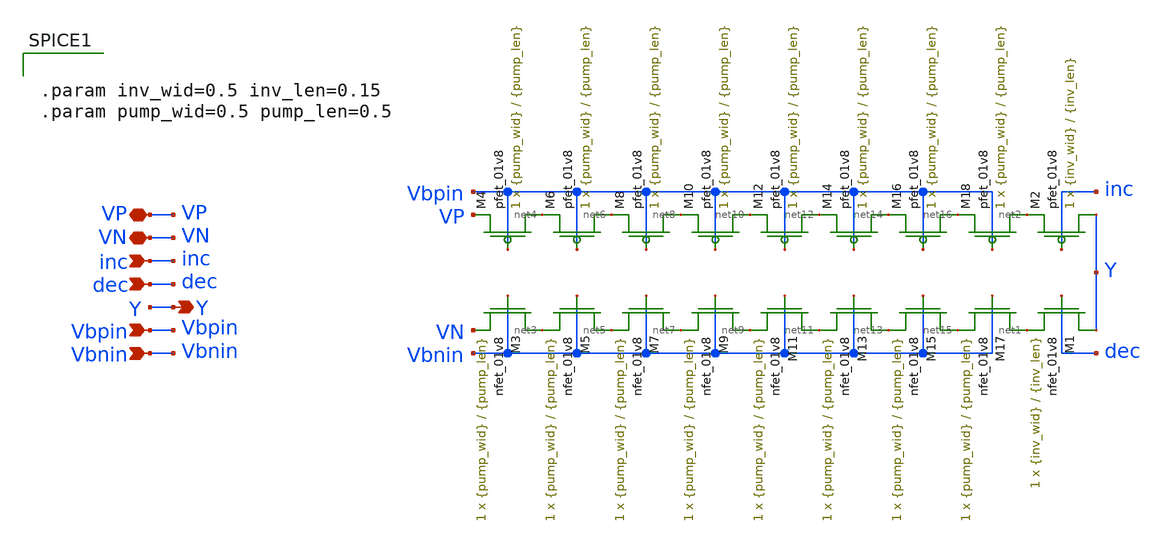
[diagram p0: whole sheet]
** sch_path: LDS/LDS_ipump.sch
**.subckt LDS_ipump VN VP Y Vbpin inc Vbnin dec
*.iopin VN
*.iopin VP
*.opin Y
*.ipin Vbpin
*.ipin inc
*.ipin Vbnin
*.ipin dec
XM1 Y dec net1 VN sky130_fd_pr__nfet_01v8 L={inv_len} W={inv_wid} nf=1 ad='int((nf+1)/2) * W/nf * 0.29'
+ as='int((nf+2)/2) * W/nf * 0.29' pd='2*int((nf+1)/2) * (W/nf + 0.29)' ps='2*int((nf+2)/2) * (W/nf + 0.29)'
+ nrd='0.29 / W' nrs='0.29 / W' sa=0 sb=0 sd=0 mult=1 m=1
XM2 Y inc net2 VP sky130_fd_pr__pfet_01v8 L={inv_len} W={inv_wid} nf=1 ad='int((nf+1)/2) * W/nf * 0.29'
+ as='int((nf+2)/2) * W/nf * 0.29' pd='2*int((nf+1)/2) * (W/nf + 0.29)' ps='2*int((nf+2)/2) * (W/nf + 0.29)'
+ nrd='0.29 / W' nrs='0.29 / W' sa=0 sb=0 sd=0 mult=1 m=1
XM3 net3 Vbnin VN VN sky130_fd_pr__nfet_01v8 L={pump_len} W={pump_wid} nf=1 ad='int((nf+1)/2) * W/nf * 0.29'
+ as='int((nf+2)/2) * W/nf * 0.29' pd='2*int((nf+1)/2) * (W/nf + 0.29)' ps='2*int((nf+2)/2) * (W/nf + 0.29)'
+ nrd='0.29 / W' nrs='0.29 / W' sa=0 sb=0 sd=0 mult=1 m=1
XM4 net4 Vbpin VP VP sky130_fd_pr__pfet_01v8 L={pump_len} W={pump_wid} nf=1 ad='int((nf+1)/2) * W/nf * 0.29'
+ as='int((nf+2)/2) * W/nf * 0.29' pd='2*int((nf+1)/2) * (W/nf + 0.29)' ps='2*int((nf+2)/2) * (W/nf + 0.29)'
+ nrd='0.29 / W' nrs='0.29 / W' sa=0 sb=0 sd=0 mult=1 m=1
XM5 net5 Vbnin net3 VN sky130_fd_pr__nfet_01v8 L={pump_len} W={pump_wid} nf=1 ad='int((nf+1)/2) * W/nf * 0.29'
+ as='int((nf+2)/2) * W/nf * 0.29' pd='2*int((nf+1)/2) * (W/nf + 0.29)' ps='2*int((nf+2)/2) * (W/nf + 0.29)'
+ nrd='0.29 / W' nrs='0.29 / W' sa=0 sb=0 sd=0 mult=1 m=1
XM6 net6 Vbpin net4 VP sky130_fd_pr__pfet_01v8 L={pump_len} W={pump_wid} nf=1 ad='int((nf+1)/2) * W/nf * 0.29'
+ as='int((nf+2)/2) * W/nf * 0.29' pd='2*int((nf+1)/2) * (W/nf + 0.29)' ps='2*int((nf+2)/2) * (W/nf + 0.29)'
+ nrd='0.29 / W' nrs='0.29 / W' sa=0 sb=0 sd=0 mult=1 m=1
XM7 net7 Vbnin net5 VN sky130_fd_pr__nfet_01v8 L={pump_len} W={pump_wid} nf=1 ad='int((nf+1)/2) * W/nf * 0.29'
+ as='int((nf+2)/2) * W/nf * 0.29' pd='2*int((nf+1)/2) * (W/nf + 0.29)' ps='2*int((nf+2)/2) * (W/nf + 0.29)'
+ nrd='0.29 / W' nrs='0.29 / W' sa=0 sb=0 sd=0 mult=1 m=1
XM8 net8 Vbpin net6 VP sky130_fd_pr__pfet_01v8 L={pump_len} W={pump_wid} nf=1 ad='int((nf+1)/2) * W/nf * 0.29'
+ as='int((nf+2)/2) * W/nf * 0.29' pd='2*int((nf+1)/2) * (W/nf + 0.29)' ps='2*int((nf+2)/2) * (W/nf + 0.29)'
+ nrd='0.29 / W' nrs='0.29 / W' sa=0 sb=0 sd=0 mult=1 m=1
XM9 net9 Vbnin net7 VN sky130_fd_pr__nfet_01v8 L={pump_len} W={pump_wid} nf=1 ad='int((nf+1)/2) * W/nf * 0.29'
+ as='int((nf+2)/2) * W/nf * 0.29' pd='2*int((nf+1)/2) * (W/nf + 0.29)' ps='2*int((nf+2)/2) * (W/nf + 0.29)'
+ nrd='0.29 / W' nrs='0.29 / W' sa=0 sb=0 sd=0 mult=1 m=1
XM10 net10 Vbpin net8 VP sky130_fd_pr__pfet_01v8 L={pump_len} W={pump_wid} nf=1 ad='int((nf+1)/2) * W/nf * 0.29'
+ as='int((nf+2)/2) * W/nf * 0.29' pd='2*int((nf+1)/2) * (W/nf + 0.29)' ps='2*int((nf+2)/2) * (W/nf + 0.29)'
+ nrd='0.29 / W' nrs='0.29 / W' sa=0 sb=0 sd=0 mult=1 m=1
XM11 net11 Vbnin net9 VN sky130_fd_pr__nfet_01v8 L={pump_len} W={pump_wid} nf=1 ad='int((nf+1)/2) * W/nf * 0.29'
+ as='int((nf+2)/2) * W/nf * 0.29' pd='2*int((nf+1)/2) * (W/nf + 0.29)' ps='2*int((nf+2)/2) * (W/nf + 0.29)'
+ nrd='0.29 / W' nrs='0.29 / W' sa=0 sb=0 sd=0 mult=1 m=1
XM12 net12 Vbpin net10 VP sky130_fd_pr__pfet_01v8 L={pump_len} W={pump_wid} nf=1 ad='int((nf+1)/2) * W/nf * 0.29'
+ as='int((nf+2)/2) * W/nf * 0.29' pd='2*int((nf+1)/2) * (W/nf + 0.29)' ps='2*int((nf+2)/2) * (W/nf + 0.29)'
+ nrd='0.29 / W' nrs='0.29 / W' sa=0 sb=0 sd=0 mult=1 m=1
XM13 net13 Vbnin net11 VN sky130_fd_pr__nfet_01v8 L={pump_len} W={pump_wid} nf=1 ad='int((nf+1)/2) * W/nf * 0.29'
+ as='int((nf+2)/2) * W/nf * 0.29' pd='2*int((nf+1)/2) * (W/nf + 0.29)' ps='2*int((nf+2)/2) * (W/nf + 0.29)'
+ nrd='0.29 / W' nrs='0.29 / W' sa=0 sb=0 sd=0 mult=1 m=1
XM14 net14 Vbpin net12 VP sky130_fd_pr__pfet_01v8 L={pump_len} W={pump_wid} nf=1 ad='int((nf+1)/2) * W/nf * 0.29'
+ as='int((nf+2)/2) * W/nf * 0.29' pd='2*int((nf+1)/2) * (W/nf + 0.29)' ps='2*int((nf+2)/2) * (W/nf + 0.29)'
+ nrd='0.29 / W' nrs='0.29 / W' sa=0 sb=0 sd=0 mult=1 m=1
XM15 net15 Vbnin net13 VN sky130_fd_pr__nfet_01v8 L={pump_len} W={pump_wid} nf=1 ad='int((nf+1)/2) * W/nf * 0.29'
+ as='int((nf+2)/2) * W/nf * 0.29' pd='2*int((nf+1)/2) * (W/nf + 0.29)' ps='2*int((nf+2)/2) * (W/nf + 0.29)'
+ nrd='0.29 / W' nrs='0.29 / W' sa=0 sb=0 sd=0 mult=1 m=1
XM16 net16 Vbpin net14 VP sky130_fd_pr__pfet_01v8 L={pump_len} W={pump_wid} nf=1 ad='int((nf+1)/2) * W/nf * 0.29'
+ as='int((nf+2)/2) * W/nf * 0.29' pd='2*int((nf+1)/2) * (W/nf + 0.29)' ps='2*int((nf+2)/2) * (W/nf + 0.29)'
+ nrd='0.29 / W' nrs='0.29 / W' sa=0 sb=0 sd=0 mult=1 m=1
XM17 net1 Vbnin net15 VN sky130_fd_pr__nfet_01v8 L={pump_len} W={pump_wid} nf=1 ad='int((nf+1)/2) * W/nf * 0.29'
+ as='int((nf+2)/2) * W/nf * 0.29' pd='2*int((nf+1)/2) * (W/nf + 0.29)' ps='2*int((nf+2)/2) * (W/nf + 0.29)'
+ nrd='0.29 / W' nrs='0.29 / W' sa=0 sb=0 sd=0 mult=1 m=1
XM18 net2 Vbpin net16 VP sky130_fd_pr__pfet_01v8 L={pump_len} W={pump_wid} nf=1 ad='int((nf+1)/2) * W/nf * 0.29'
+ as='int((nf+2)/2) * W/nf * 0.29' pd='2*int((nf+1)/2) * (W/nf + 0.29)' ps='2*int((nf+2)/2) * (W/nf + 0.29)'
+ nrd='0.29 / W' nrs='0.29 / W' sa=0 sb=0 sd=0 mult=1 m=1
**** begin user architecture code


.param inv_wid=0.5 inv_len=0.15
.param pump_wid=0.5 pump_len=0.5


**** end user architecture code
**.ends
.end
